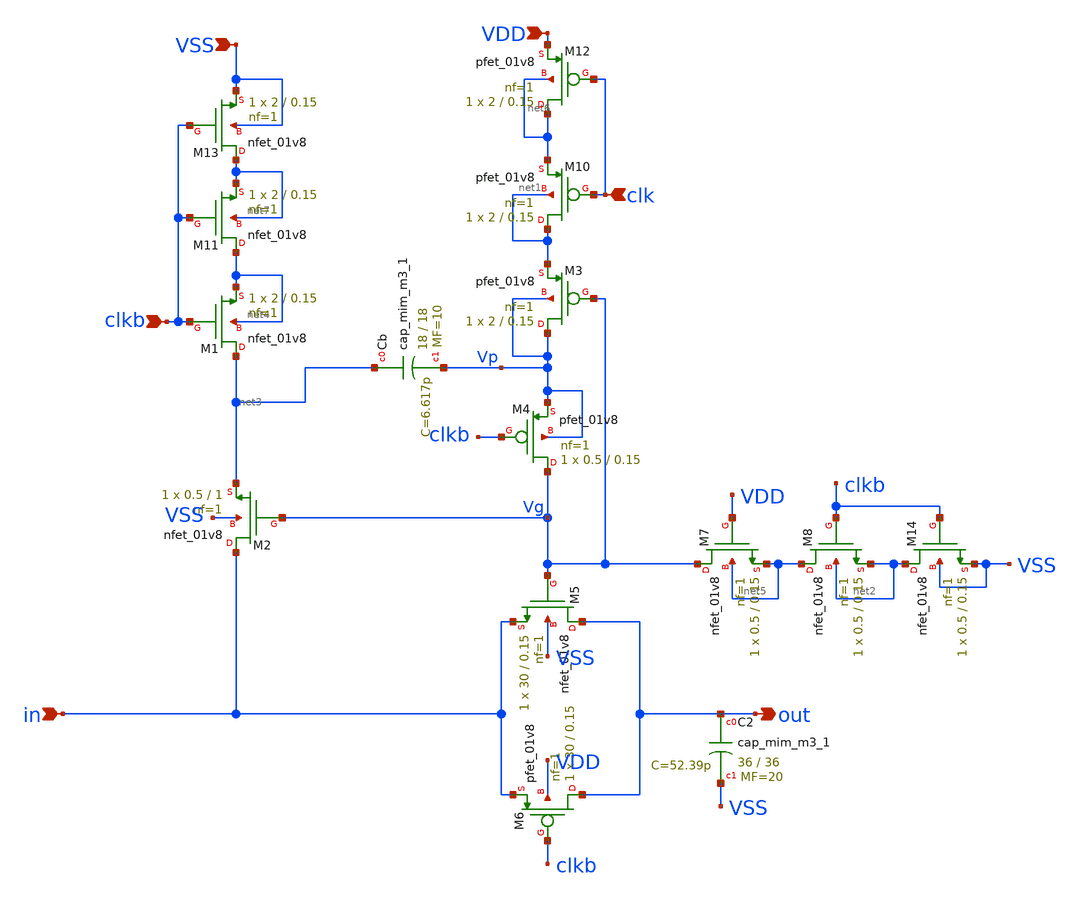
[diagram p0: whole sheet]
** sch_path: bootstrapped_switch_SH.sch
**.subckt bootstrapped_switch_SH in out VSS VDD clkb clk
*.ipin in
*.opin out
*.ipin VSS
*.ipin VDD
*.ipin clkb
*.ipin clk
XM1 net3 clkb net4 net4 sky130_fd_pr__nfet_01v8 L=0.15 W=2 nf=1 ad='int((nf+1)/2) * W/nf * 0.29' as='int((nf+2)/2) * W/nf * 0.29'
+ pd='2*int((nf+1)/2) * (W/nf + 0.29)' ps='2*int((nf+2)/2) * (W/nf + 0.29)' nrd='0.29 / W' nrs='0.29 / W'
+ sa=0 sb=0 sd=0 mult=1 m=1
XM2 in Vg net3 VSS sky130_fd_pr__nfet_01v8 L=1 W=0.5 nf=1 ad='int((nf+1)/2) * W/nf * 0.29' as='int((nf+2)/2) * W/nf * 0.29'
+ pd='2*int((nf+1)/2) * (W/nf + 0.29)' ps='2*int((nf+2)/2) * (W/nf + 0.29)' nrd='0.29 / W' nrs='0.29 / W'
+ sa=0 sb=0 sd=0 mult=1 m=1
XM3 Vp Vg net1 Vp sky130_fd_pr__pfet_01v8 L=0.15 W=2 nf=1 ad='int((nf+1)/2) * W/nf * 0.29' as='int((nf+2)/2) * W/nf * 0.29'
+ pd='2*int((nf+1)/2) * (W/nf + 0.29)' ps='2*int((nf+2)/2) * (W/nf + 0.29)' nrd='0.29 / W' nrs='0.29 / W'
+ sa=0 sb=0 sd=0 mult=1 m=1
XM5 out Vg in VSS sky130_fd_pr__nfet_01v8 L=0.15 W=30 nf=1 ad='int((nf+1)/2) * W/nf * 0.29' as='int((nf+2)/2) * W/nf * 0.29'
+ pd='2*int((nf+1)/2) * (W/nf + 0.29)' ps='2*int((nf+2)/2) * (W/nf + 0.29)' nrd='0.29 / W' nrs='0.29 / W'
+ sa=0 sb=0 sd=0 mult=1 m=1
XM6 out clkb in VDD sky130_fd_pr__pfet_01v8 L=0.15 W=30 nf=1 ad='int((nf+1)/2) * W/nf * 0.29' as='int((nf+2)/2) * W/nf * 0.29'
+ pd='2*int((nf+1)/2) * (W/nf + 0.29)' ps='2*int((nf+2)/2) * (W/nf + 0.29)' nrd='0.29 / W' nrs='0.29 / W'
+ sa=0 sb=0 sd=0 mult=1 m=1
XM8 net5 clkb net2 net2 sky130_fd_pr__nfet_01v8 L=0.15 W=0.5 nf=1 ad='int((nf+1)/2) * W/nf * 0.29' as='int((nf+2)/2) * W/nf * 0.29'
+ pd='2*int((nf+1)/2) * (W/nf + 0.29)' ps='2*int((nf+2)/2) * (W/nf + 0.29)' nrd='0.29 / W' nrs='0.29 / W'
+ sa=0 sb=0 sd=0 mult=1 m=1
XCb net3 Vp sky130_fd_pr__cap_mim_m3_1 W=18 L=18 MF=10 m=10
XM7 Vg VDD net5 net5 sky130_fd_pr__nfet_01v8 L=0.15 W=0.5 nf=1 ad='int((nf+1)/2) * W/nf * 0.29' as='int((nf+2)/2) * W/nf * 0.29'
+ pd='2*int((nf+1)/2) * (W/nf + 0.29)' ps='2*int((nf+2)/2) * (W/nf + 0.29)' nrd='0.29 / W' nrs='0.29 / W'
+ sa=0 sb=0 sd=0 mult=1 m=1
XM4 Vg clkb Vp Vp sky130_fd_pr__pfet_01v8 L=0.15 W=0.5 nf=1 ad='int((nf+1)/2) * W/nf * 0.29' as='int((nf+2)/2) * W/nf * 0.29'
+ pd='2*int((nf+1)/2) * (W/nf + 0.29)' ps='2*int((nf+2)/2) * (W/nf + 0.29)' nrd='0.29 / W' nrs='0.29 / W'
+ sa=0 sb=0 sd=0 mult=1 m=1
XM10 net1 clk net6 net1 sky130_fd_pr__pfet_01v8 L=0.15 W=2 nf=1 ad='int((nf+1)/2) * W/nf * 0.29' as='int((nf+2)/2) * W/nf * 0.29'
+ pd='2*int((nf+1)/2) * (W/nf + 0.29)' ps='2*int((nf+2)/2) * (W/nf + 0.29)' nrd='0.29 / W' nrs='0.29 / W'
+ sa=0 sb=0 sd=0 mult=1 m=1
XM11 net4 clkb net7 net7 sky130_fd_pr__nfet_01v8 L=0.15 W=2 nf=1 ad='int((nf+1)/2) * W/nf * 0.29' as='int((nf+2)/2) * W/nf * 0.29'
+ pd='2*int((nf+1)/2) * (W/nf + 0.29)' ps='2*int((nf+2)/2) * (W/nf + 0.29)' nrd='0.29 / W' nrs='0.29 / W'
+ sa=0 sb=0 sd=0 mult=1 m=1
XM12 net6 clk VDD net6 sky130_fd_pr__pfet_01v8 L=0.15 W=2 nf=1 ad='int((nf+1)/2) * W/nf * 0.29' as='int((nf+2)/2) * W/nf * 0.29'
+ pd='2*int((nf+1)/2) * (W/nf + 0.29)' ps='2*int((nf+2)/2) * (W/nf + 0.29)' nrd='0.29 / W' nrs='0.29 / W'
+ sa=0 sb=0 sd=0 mult=1 m=1
XM13 net7 clkb VSS VSS sky130_fd_pr__nfet_01v8 L=0.15 W=2 nf=1 ad='int((nf+1)/2) * W/nf * 0.29' as='int((nf+2)/2) * W/nf * 0.29'
+ pd='2*int((nf+1)/2) * (W/nf + 0.29)' ps='2*int((nf+2)/2) * (W/nf + 0.29)' nrd='0.29 / W' nrs='0.29 / W'
+ sa=0 sb=0 sd=0 mult=1 m=1
XM14 net2 clkb VSS VSS sky130_fd_pr__nfet_01v8 L=0.15 W=0.5 nf=1 ad='int((nf+1)/2) * W/nf * 0.29' as='int((nf+2)/2) * W/nf * 0.29'
+ pd='2*int((nf+1)/2) * (W/nf + 0.29)' ps='2*int((nf+2)/2) * (W/nf + 0.29)' nrd='0.29 / W' nrs='0.29 / W'
+ sa=0 sb=0 sd=0 mult=1 m=1
XC2 out VSS sky130_fd_pr__cap_mim_m3_1 W=36 L=36 MF=20 m=20
**.ends
.end
